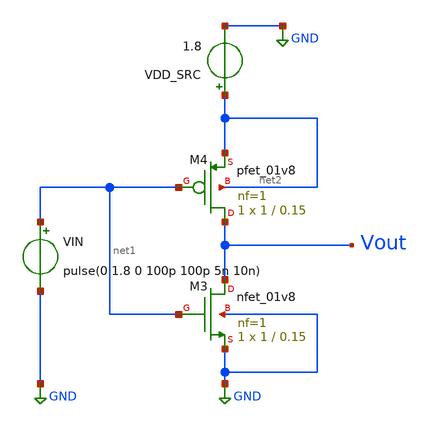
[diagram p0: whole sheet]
** sch_path: verification/xschem/sram_6t_bitcell.sch
**.subckt sram_6t_bitcell
VIN net1 GND pulse(0 1.8 0 100p 100p 5n 10n)
VDD_SRC net2 GND 1.8
XM3 Vout net1 GND GND sky130_fd_pr__nfet_01v8 L=0.15 W=1 nf=1 ad='int((1 + 1)/2) * 1 / 1 * 0.29' as='int((1 + 2)/2) * 1 / 1 * 0.29'
+ pd='2*int((1 + 1)/2) * (1 / 1 + 0.29)' ps='2*int((1 + 2)/2) * (1 / 1 + 0.29)' nrd='0.29 / 1 ' nrs='0.29 / 1 '
+ sa=0 sb=0 sd=0 mult=1 m=1
XM4 Vout net1 net2 net2 sky130_fd_pr__pfet_01v8 L=0.15 W=1 nf=1 ad='int((nf+1)/2) * W/nf * 0.29' as='int((nf+2)/2) * W/nf * 0.29'
+ pd='2*int((nf+1)/2) * (W/nf + 0.29)' ps='2*int((nf+2)/2) * (W/nf + 0.29)' nrd='0.29 / W' nrs='0.29 / W'
+ sa=0 sb=0 sd=0 mult=1 m=1
**** begin user architecture code


.lib /home/devdutt/gf/pdk/sky130A/libs.tech/ngspice/sky130.lib.spice tt

.tran 10p 50n

.control
run
plot v(net1) v(vout)
.endc

**** end user architecture code
**.ends
.GLOBAL GND
.end
